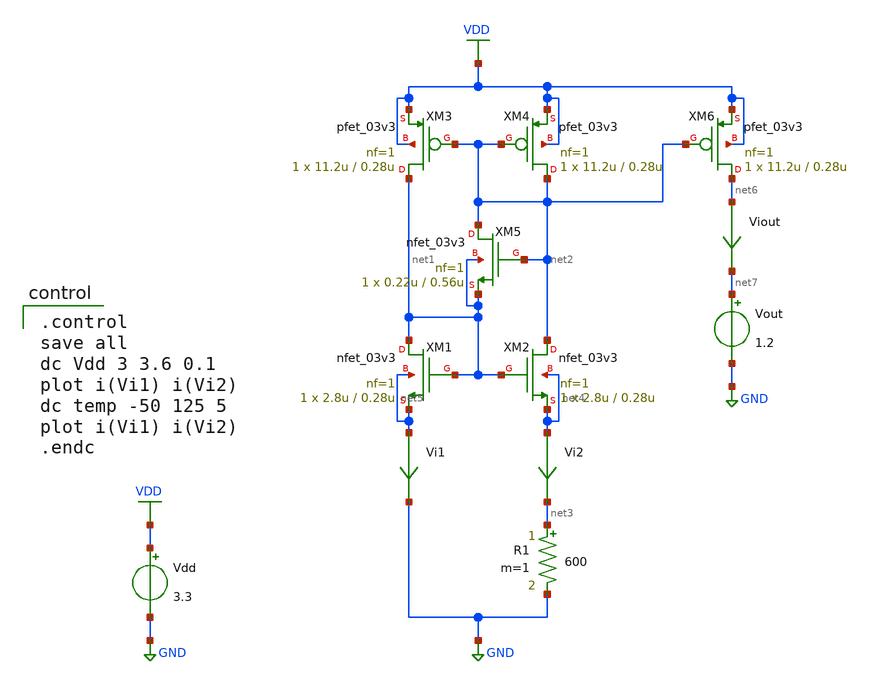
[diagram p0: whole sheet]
** sch_path: current-source/cs-widlar-mod.sch
**.subckt cs-widlar-mod
Vdd VDD GND 3.3
R1 net3 GND 600 m=1
XM1 net1 net1 net5 net5 nfet_03v3 L=0.28u W=2.8u nf=1 ad='int((nf+1)/2) * W/nf * 0.18u' as='int((nf+2)/2) * W/nf * 0.18u'
+ pd='2*int((nf+1)/2) * (W/nf + 0.18u)' ps='2*int((nf+2)/2) * (W/nf + 0.18u)' nrd='0.18u / W' nrs='0.18u / W'
+ sa=0 sb=0 sd=0 m=1
XM2 net2 net1 net4 net4 nfet_03v3 L=0.28u W=2.8u nf=1 ad='int((nf+1)/2) * W/nf * 0.18u' as='int((nf+2)/2) * W/nf * 0.18u'
+ pd='2*int((nf+1)/2) * (W/nf + 0.18u)' ps='2*int((nf+2)/2) * (W/nf + 0.18u)' nrd='0.18u / W' nrs='0.18u / W'
+ sa=0 sb=0 sd=0 m=1
XM3 net1 net2 VDD VDD pfet_03v3 L=0.28u W=11.2u nf=1 ad='int((nf+1)/2) * W/nf * 0.18u' as='int((nf+2)/2) * W/nf * 0.18u'
+ pd='2*int((nf+1)/2) * (W/nf + 0.18u)' ps='2*int((nf+2)/2) * (W/nf + 0.18u)' nrd='0.18u / W' nrs='0.18u / W'
+ sa=0 sb=0 sd=0 m=1
XM4 net2 net2 VDD VDD pfet_03v3 L=0.28u W=11.2u nf=1 ad='int((nf+1)/2) * W/nf * 0.18u' as='int((nf+2)/2) * W/nf * 0.18u'
+ pd='2*int((nf+1)/2) * (W/nf + 0.18u)' ps='2*int((nf+2)/2) * (W/nf + 0.18u)' nrd='0.18u / W' nrs='0.18u / W'
+ sa=0 sb=0 sd=0 m=1
Vi1 net5 GND 0
.save i(vi1)
Vi2 net4 net3 0
.save i(vi2)
XM5 net2 net2 net1 net1 nfet_03v3 L=0.56u W=0.22u nf=1 ad='int((nf+1)/2) * W/nf * 0.18u' as='int((nf+2)/2) * W/nf * 0.18u'
+ pd='2*int((nf+1)/2) * (W/nf + 0.18u)' ps='2*int((nf+2)/2) * (W/nf + 0.18u)' nrd='0.18u / W' nrs='0.18u / W'
+ sa=0 sb=0 sd=0 m=1
XM6 net6 net2 VDD VDD pfet_03v3 L=0.28u W=11.2u nf=1 ad='int((nf+1)/2) * W/nf * 0.18u' as='int((nf+2)/2) * W/nf * 0.18u'
+ pd='2*int((nf+1)/2) * (W/nf + 0.18u)' ps='2*int((nf+2)/2) * (W/nf + 0.18u)' nrd='0.18u / W' nrs='0.18u / W'
+ sa=0 sb=0 sd=0 m=1
Viout net6 net7 0
.save i(viout)
Vout net7 GND 1.2
**** begin user architecture code

.include $::180MCU_MODELS/design.ngspice
.lib $::180MCU_MODELS/sm141064.ngspice typical
.lib $::180MCU_MODELS/sm141064.ngspice res_typical
.lib $::180MCU_MODELS/sm141064.ngspice moscap_typical
.lib $::180MCU_MODELS/sm141064.ngspice bjt_typical
* .lib $::180MCU_MODELS/sm141064.ngspice res_statistical


.control
save all
dc Vdd 3 3.6 0.1
plot i(Vi1) i(Vi2)
dc temp -50 125 5
plot i(Vi1) i(Vi2)
.endc

**** end user architecture code
**.ends
.GLOBAL GND
.GLOBAL VDD
.end
